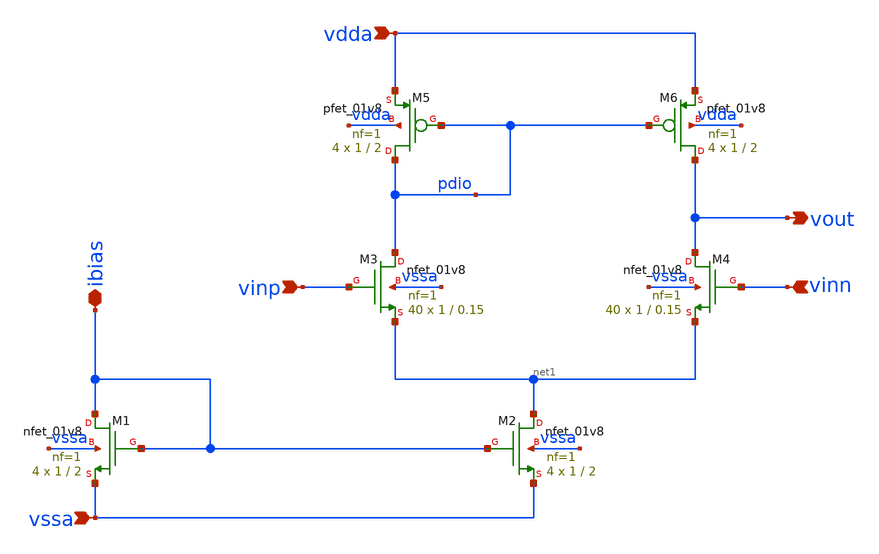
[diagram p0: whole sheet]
** sch_path: Analysing_DCOPs_in_xschem_ngpisce_in_SW130/OTA.sch
**.subckt OTA ibias vdda vssa vinp vinn vout
*.iopin ibias
*.ipin vdda
*.ipin vssa
*.ipin vinp
*.ipin vinn
*.opin vout
XM3 pdio vinp net1 vssa sky130_fd_pr__nfet_01v8 L=0.15 W=1 nf=1 ad='int((nf+1)/2) * W/nf * 0.29' as='int((nf+2)/2) * W/nf * 0.29'
+ pd='2*int((nf+1)/2) * (W/nf + 0.29)' ps='2*int((nf+2)/2) * (W/nf + 0.29)' nrd='0.29 / W' nrs='0.29 / W'
+ sa=0 sb=0 sd=0 mult=40 m=40
XM4 vout vinn net1 vssa sky130_fd_pr__nfet_01v8 L=0.15 W=1 nf=1 ad='int((nf+1)/2) * W/nf * 0.29' as='int((nf+2)/2) * W/nf * 0.29'
+ pd='2*int((nf+1)/2) * (W/nf + 0.29)' ps='2*int((nf+2)/2) * (W/nf + 0.29)' nrd='0.29 / W' nrs='0.29 / W'
+ sa=0 sb=0 sd=0 mult=40 m=40
XM5 pdio pdio vdda vdda sky130_fd_pr__pfet_01v8 L=2 W=1 nf=1 ad='int((nf+1)/2) * W/nf * 0.29' as='int((nf+2)/2) * W/nf * 0.29'
+ pd='2*int((nf+1)/2) * (W/nf + 0.29)' ps='2*int((nf+2)/2) * (W/nf + 0.29)' nrd='0.29 / W' nrs='0.29 / W'
+ sa=0 sb=0 sd=0 mult=4 m=4
XM2 net1 ibias vssa vssa sky130_fd_pr__nfet_01v8 L=2 W=1 nf=1 ad='int((nf+1)/2) * W/nf * 0.29' as='int((nf+2)/2) * W/nf * 0.29'
+ pd='2*int((nf+1)/2) * (W/nf + 0.29)' ps='2*int((nf+2)/2) * (W/nf + 0.29)' nrd='0.29 / W' nrs='0.29 / W'
+ sa=0 sb=0 sd=0 mult=4 m=4
XM1 ibias ibias vssa vssa sky130_fd_pr__nfet_01v8 L=2 W=1 nf=1 ad='int((nf+1)/2) * W/nf * 0.29' as='int((nf+2)/2) * W/nf * 0.29'
+ pd='2*int((nf+1)/2) * (W/nf + 0.29)' ps='2*int((nf+2)/2) * (W/nf + 0.29)' nrd='0.29 / W' nrs='0.29 / W'
+ sa=0 sb=0 sd=0 mult=4 m=4
XM6 vout pdio vdda vdda sky130_fd_pr__pfet_01v8 L=2 W=1 nf=1 ad='int((nf+1)/2) * W/nf * 0.29' as='int((nf+2)/2) * W/nf * 0.29'
+ pd='2*int((nf+1)/2) * (W/nf + 0.29)' ps='2*int((nf+2)/2) * (W/nf + 0.29)' nrd='0.29 / W' nrs='0.29 / W'
+ sa=0 sb=0 sd=0 mult=4 m=4
**.ends
.end
